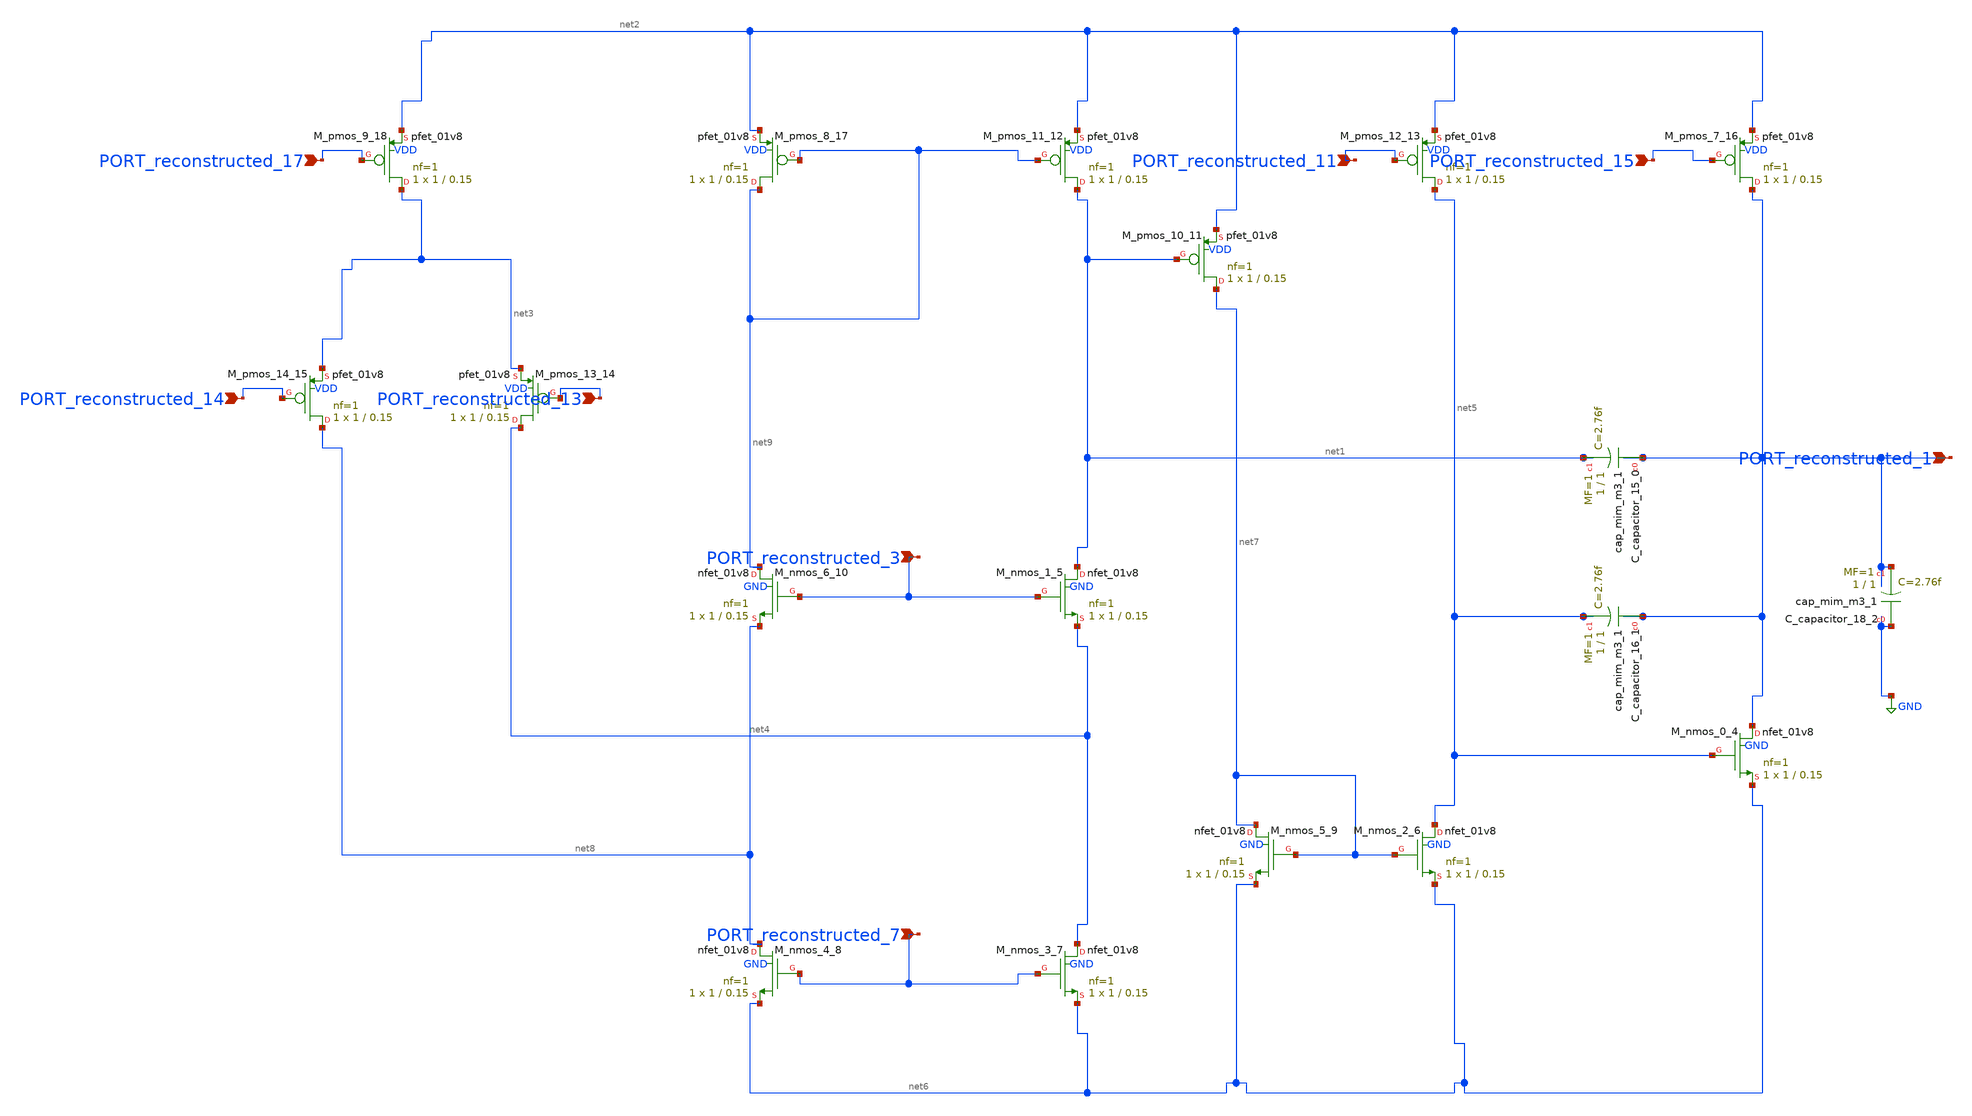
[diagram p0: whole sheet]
** sch_path: schematics/10_1109_ACCESS_2019_2940560_02_001.sch
**.subckt 10_1109_ACCESS_2019_2940560_02_001 PORT_reconstructed_14 PORT_reconstructed_13
*+ PORT_reconstructed_1 PORT_reconstructed_7 PORT_reconstructed_15 PORT_reconstructed_17 PORT_reconstructed_3
*+ PORT_reconstructed_11
*.ipin PORT_reconstructed_14
*.ipin PORT_reconstructed_13
*.ipin PORT_reconstructed_1
*.ipin PORT_reconstructed_7
*.ipin PORT_reconstructed_15
*.ipin PORT_reconstructed_17
*.ipin PORT_reconstructed_3
*.ipin PORT_reconstructed_11
XC_capacitor_15_0 PORT_reconstructed_1 net1 sky130_fd_pr__cap_mim_m3_1 W=1 L=1 MF=1 m=1
XC_capacitor_16_1 PORT_reconstructed_1 net5 sky130_fd_pr__cap_mim_m3_1 W=1 L=1 MF=1 m=1
XC_capacitor_18_2 GND PORT_reconstructed_1 sky130_fd_pr__cap_mim_m3_1 W=1 L=1 MF=1 m=1
XM_nmos_0_4 PORT_reconstructed_1 net5 net6 GND sky130_fd_pr__nfet_01v8 L=0.15 W=1 nf=1 ad='int((1 + 1)/2) * 1 / 1 * 0.29'
+ as='int((1 + 2)/2) * 1 / 1 * 0.29' pd='2*int((1 + 1)/2) * (1 / 1 + 0.29)' ps='2*int((1 + 2)/2) * (1 / 1 + 0.29)'
+ nrd='0.29 / 1 ' nrs='0.29 / 1 ' sa=0 sb=0 sd=0 mult=1 m=1
XM_nmos_1_5 net1 PORT_reconstructed_3 net4 GND sky130_fd_pr__nfet_01v8 L=0.15 W=1 nf=1 ad='int((1 + 1)/2) * 1 / 1 * 0.29'
+ as='int((1 + 2)/2) * 1 / 1 * 0.29' pd='2*int((1 + 1)/2) * (1 / 1 + 0.29)' ps='2*int((1 + 2)/2) * (1 / 1 + 0.29)'
+ nrd='0.29 / 1 ' nrs='0.29 / 1 ' sa=0 sb=0 sd=0 mult=1 m=1
XM_nmos_2_6 net5 net7 net6 GND sky130_fd_pr__nfet_01v8 L=0.15 W=1 nf=1 ad='int((1 + 1)/2) * 1 / 1 * 0.29'
+ as='int((1 + 2)/2) * 1 / 1 * 0.29' pd='2*int((1 + 1)/2) * (1 / 1 + 0.29)' ps='2*int((1 + 2)/2) * (1 / 1 + 0.29)'
+ nrd='0.29 / 1 ' nrs='0.29 / 1 ' sa=0 sb=0 sd=0 mult=1 m=1
XM_nmos_3_7 net4 PORT_reconstructed_7 net6 GND sky130_fd_pr__nfet_01v8 L=0.15 W=1 nf=1 ad='int((1 + 1)/2) * 1 / 1 * 0.29'
+ as='int((1 + 2)/2) * 1 / 1 * 0.29' pd='2*int((1 + 1)/2) * (1 / 1 + 0.29)' ps='2*int((1 + 2)/2) * (1 / 1 + 0.29)'
+ nrd='0.29 / 1 ' nrs='0.29 / 1 ' sa=0 sb=0 sd=0 mult=1 m=1
XM_nmos_4_8 net8 PORT_reconstructed_7 net6 GND sky130_fd_pr__nfet_01v8 L=0.15 W=1 nf=1 ad='int((1 + 1)/2) * 1 / 1 * 0.29'
+ as='int((1 + 2)/2) * 1 / 1 * 0.29' pd='2*int((1 + 1)/2) * (1 / 1 + 0.29)' ps='2*int((1 + 2)/2) * (1 / 1 + 0.29)'
+ nrd='0.29 / 1 ' nrs='0.29 / 1 ' sa=0 sb=0 sd=0 mult=1 m=1
XM_nmos_5_9 net7 net7 net6 GND sky130_fd_pr__nfet_01v8 L=0.15 W=1 nf=1 ad='int((1 + 1)/2) * 1 / 1 * 0.29'
+ as='int((1 + 2)/2) * 1 / 1 * 0.29' pd='2*int((1 + 1)/2) * (1 / 1 + 0.29)' ps='2*int((1 + 2)/2) * (1 / 1 + 0.29)'
+ nrd='0.29 / 1 ' nrs='0.29 / 1 ' sa=0 sb=0 sd=0 mult=1 m=1
XM_nmos_6_10 net9 PORT_reconstructed_3 net8 GND sky130_fd_pr__nfet_01v8 L=0.15 W=1 nf=1 ad='int((1 + 1)/2) * 1 / 1 * 0.29'
+ as='int((1 + 2)/2) * 1 / 1 * 0.29' pd='2*int((1 + 1)/2) * (1 / 1 + 0.29)' ps='2*int((1 + 2)/2) * (1 / 1 + 0.29)'
+ nrd='0.29 / 1 ' nrs='0.29 / 1 ' sa=0 sb=0 sd=0 mult=1 m=1
XM_pmos_10_11 net7 net1 net2 VDD sky130_fd_pr__pfet_01v8 L=0.15 W=1 nf=1 ad='int((1 + 1)/2) * 1 / 1 * 0.29'
+ as='int((1 + 2)/2) * 1 / 1 * 0.29' pd='2*int((1 + 1)/2) * (1 / 1 + 0.29)' ps='2*int((1 + 2)/2) * (1 / 1 + 0.29)'
+ nrd='0.29 / 1 ' nrs='0.29 / 1 ' sa=0 sb=0 sd=0 mult=1 m=1
XM_pmos_11_12 net1 net9 net2 VDD sky130_fd_pr__pfet_01v8 L=0.15 W=1 nf=1 ad='int((1 + 1)/2) * 1 / 1 * 0.29'
+ as='int((1 + 2)/2) * 1 / 1 * 0.29' pd='2*int((1 + 1)/2) * (1 / 1 + 0.29)' ps='2*int((1 + 2)/2) * (1 / 1 + 0.29)'
+ nrd='0.29 / 1 ' nrs='0.29 / 1 ' sa=0 sb=0 sd=0 mult=1 m=1
XM_pmos_12_13 net5 PORT_reconstructed_11 net2 VDD sky130_fd_pr__pfet_01v8 L=0.15 W=1 nf=1 ad='int((1 + 1)/2) * 1 / 1 * 0.29'
+ as='int((1 + 2)/2) * 1 / 1 * 0.29' pd='2*int((1 + 1)/2) * (1 / 1 + 0.29)' ps='2*int((1 + 2)/2) * (1 / 1 + 0.29)'
+ nrd='0.29 / 1 ' nrs='0.29 / 1 ' sa=0 sb=0 sd=0 mult=1 m=1
XM_pmos_13_14 net4 PORT_reconstructed_13 net3 VDD sky130_fd_pr__pfet_01v8 L=0.15 W=1 nf=1 ad='int((1 + 1)/2) * 1 / 1 * 0.29'
+ as='int((1 + 2)/2) * 1 / 1 * 0.29' pd='2*int((1 + 1)/2) * (1 / 1 + 0.29)' ps='2*int((1 + 2)/2) * (1 / 1 + 0.29)'
+ nrd='0.29 / 1 ' nrs='0.29 / 1 ' sa=0 sb=0 sd=0 mult=1 m=1
XM_pmos_14_15 net8 PORT_reconstructed_14 net3 VDD sky130_fd_pr__pfet_01v8 L=0.15 W=1 nf=1 ad='int((1 + 1)/2) * 1 / 1 * 0.29'
+ as='int((1 + 2)/2) * 1 / 1 * 0.29' pd='2*int((1 + 1)/2) * (1 / 1 + 0.29)' ps='2*int((1 + 2)/2) * (1 / 1 + 0.29)'
+ nrd='0.29 / 1 ' nrs='0.29 / 1 ' sa=0 sb=0 sd=0 mult=1 m=1
XM_pmos_7_16 PORT_reconstructed_1 PORT_reconstructed_15 net2 VDD sky130_fd_pr__pfet_01v8 L=0.15 W=1 nf=1
+ ad='int((1 + 1)/2) * 1 / 1 * 0.29' as='int((1 + 2)/2) * 1 / 1 * 0.29' pd='2*int((1 + 1)/2) * (1 / 1 + 0.29)'
+ ps='2*int((1 + 2)/2) * (1 / 1 + 0.29)' nrd='0.29 / 1 ' nrs='0.29 / 1 ' sa=0 sb=0 sd=0 mult=1 m=1
XM_pmos_8_17 net9 net9 net2 VDD sky130_fd_pr__pfet_01v8 L=0.15 W=1 nf=1 ad='int((1 + 1)/2) * 1 / 1 * 0.29'
+ as='int((1 + 2)/2) * 1 / 1 * 0.29' pd='2*int((1 + 1)/2) * (1 / 1 + 0.29)' ps='2*int((1 + 2)/2) * (1 / 1 + 0.29)'
+ nrd='0.29 / 1 ' nrs='0.29 / 1 ' sa=0 sb=0 sd=0 mult=1 m=1
XM_pmos_9_18 net3 PORT_reconstructed_17 net2 VDD sky130_fd_pr__pfet_01v8 L=0.15 W=1 nf=1 ad='int((1 + 1)/2) * 1 / 1 * 0.29'
+ as='int((1 + 2)/2) * 1 / 1 * 0.29' pd='2*int((1 + 1)/2) * (1 / 1 + 0.29)' ps='2*int((1 + 2)/2) * (1 / 1 + 0.29)'
+ nrd='0.29 / 1 ' nrs='0.29 / 1 ' sa=0 sb=0 sd=0 mult=1 m=1
**.ends
.GLOBAL GND
.end
